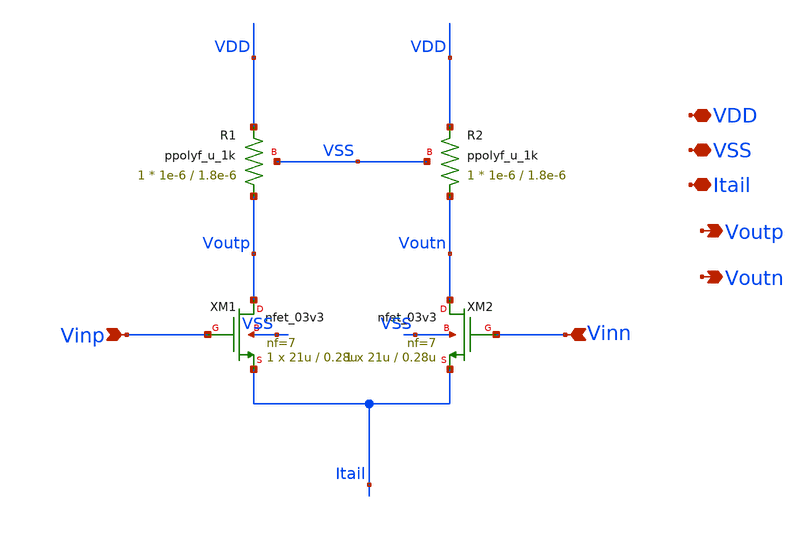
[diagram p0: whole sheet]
** sch_path: designs/output_buffer/schematic/bufferOut.sch
**.subckt bufferOut VDD Itail VSS Vinp Vinn Voutp Voutn
*.iopin VDD
*.iopin Itail
*.iopin VSS
*.ipin Vinp
*.ipin Vinn
*.opin Voutp
*.opin Voutn
XM1 Voutp Vinp Itail VSS nfet_03v3 L=0.28u W=21u nf=7 ad='int((nf+1)/2) * W/nf * 0.18u' as='int((nf+2)/2) * W/nf * 0.18u'
+ pd='2*int((nf+1)/2) * (W/nf + 0.18u)' ps='2*int((nf+2)/2) * (W/nf + 0.18u)' nrd='0.18u / W' nrs='0.18u / W'
+ sa=0 sb=0 sd=0 m=1
XM2 Voutn Vinn Itail VSS nfet_03v3 L=0.28u W=21u nf=7 ad='int((nf+1)/2) * W/nf * 0.18u' as='int((nf+2)/2) * W/nf * 0.18u'
+ pd='2*int((nf+1)/2) * (W/nf + 0.18u)' ps='2*int((nf+2)/2) * (W/nf + 0.18u)' nrd='0.18u / W' nrs='0.18u / W'
+ sa=0 sb=0 sd=0 m=1
XR1 Voutp VDD VSS ppolyf_u_1k r_width=1e-6 r_length=1.8e-6 m=1
XR2 Voutn VDD VSS ppolyf_u_1k r_width=1e-6 r_length=1.8e-6 m=1
**.ends
.end
